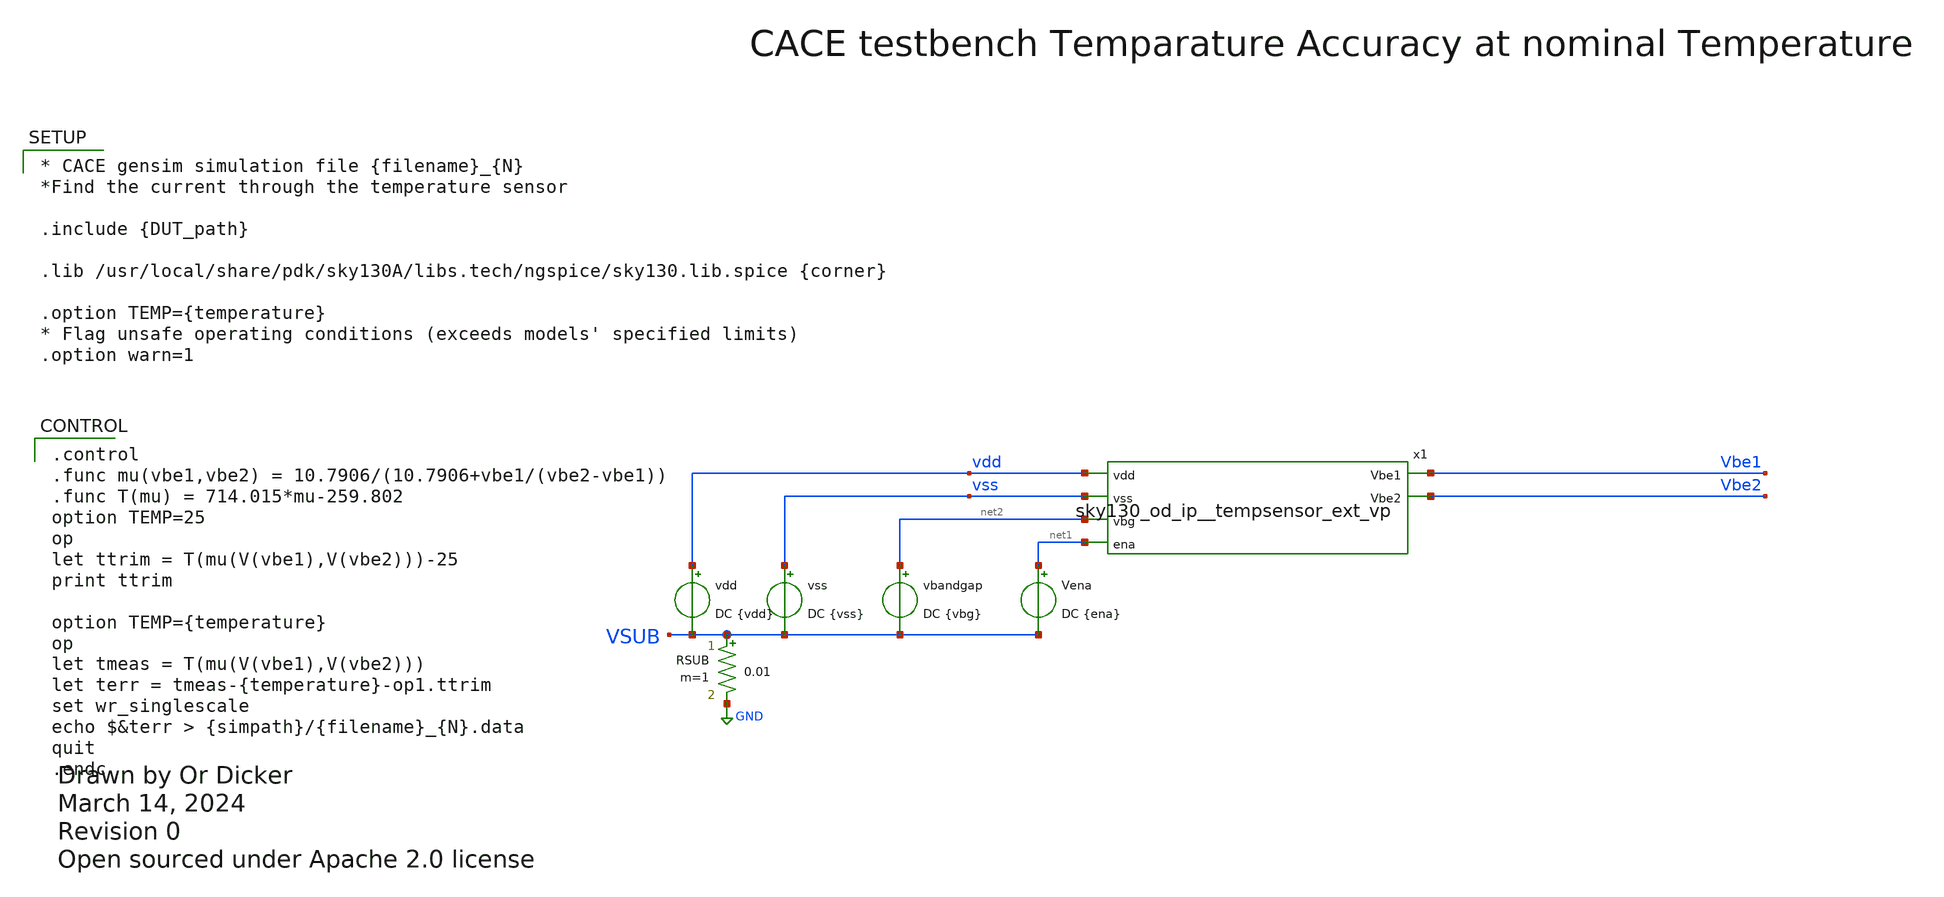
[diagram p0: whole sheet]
** sch_path: cace/templates/temperature.sch
* Open sourced under Apache 2.0 license
**.subckt temperature
vss vss VSUB DC {vss}
vdd vdd VSUB DC {vdd}
RSUB VSUB GND 0.01 m=1
Vena net1 VSUB DC {ena}
x1 vdd vss net2 Vbe1 Vbe2 net1 sky130_od_ip__tempsensor_ext_vp
vbandgap net2 VSUB DC {vbg}
**** begin user architecture code

.control
.func mu(vbe1,vbe2) = 10.7906/(10.7906+vbe1/(vbe2-vbe1))
.func T(mu) = 714.015*mu-259.802
option TEMP=25
op
let ttrim = T(mu(V(vbe1),V(vbe2)))-25
print ttrim

option TEMP={temperature}
op
let tmeas = T(mu(V(vbe1),V(vbe2)))
let terr = tmeas-{temperature}-op1.ttrim
set wr_singlescale
echo $&terr > {simpath}/{filename}_{N}.data
quit
.endc



* CACE gensim simulation file {filename}_{N}
*Find the current through the temperature sensor

.include {DUT_path}

.lib /usr/local/share/pdk/sky130A/libs.tech/ngspice/sky130.lib.spice {corner}

.option TEMP={temperature}
* Flag unsafe operating conditions (exceeds models' specified limits)
.option warn=1


**** end user architecture code
**.ends
.GLOBAL GND
.end
